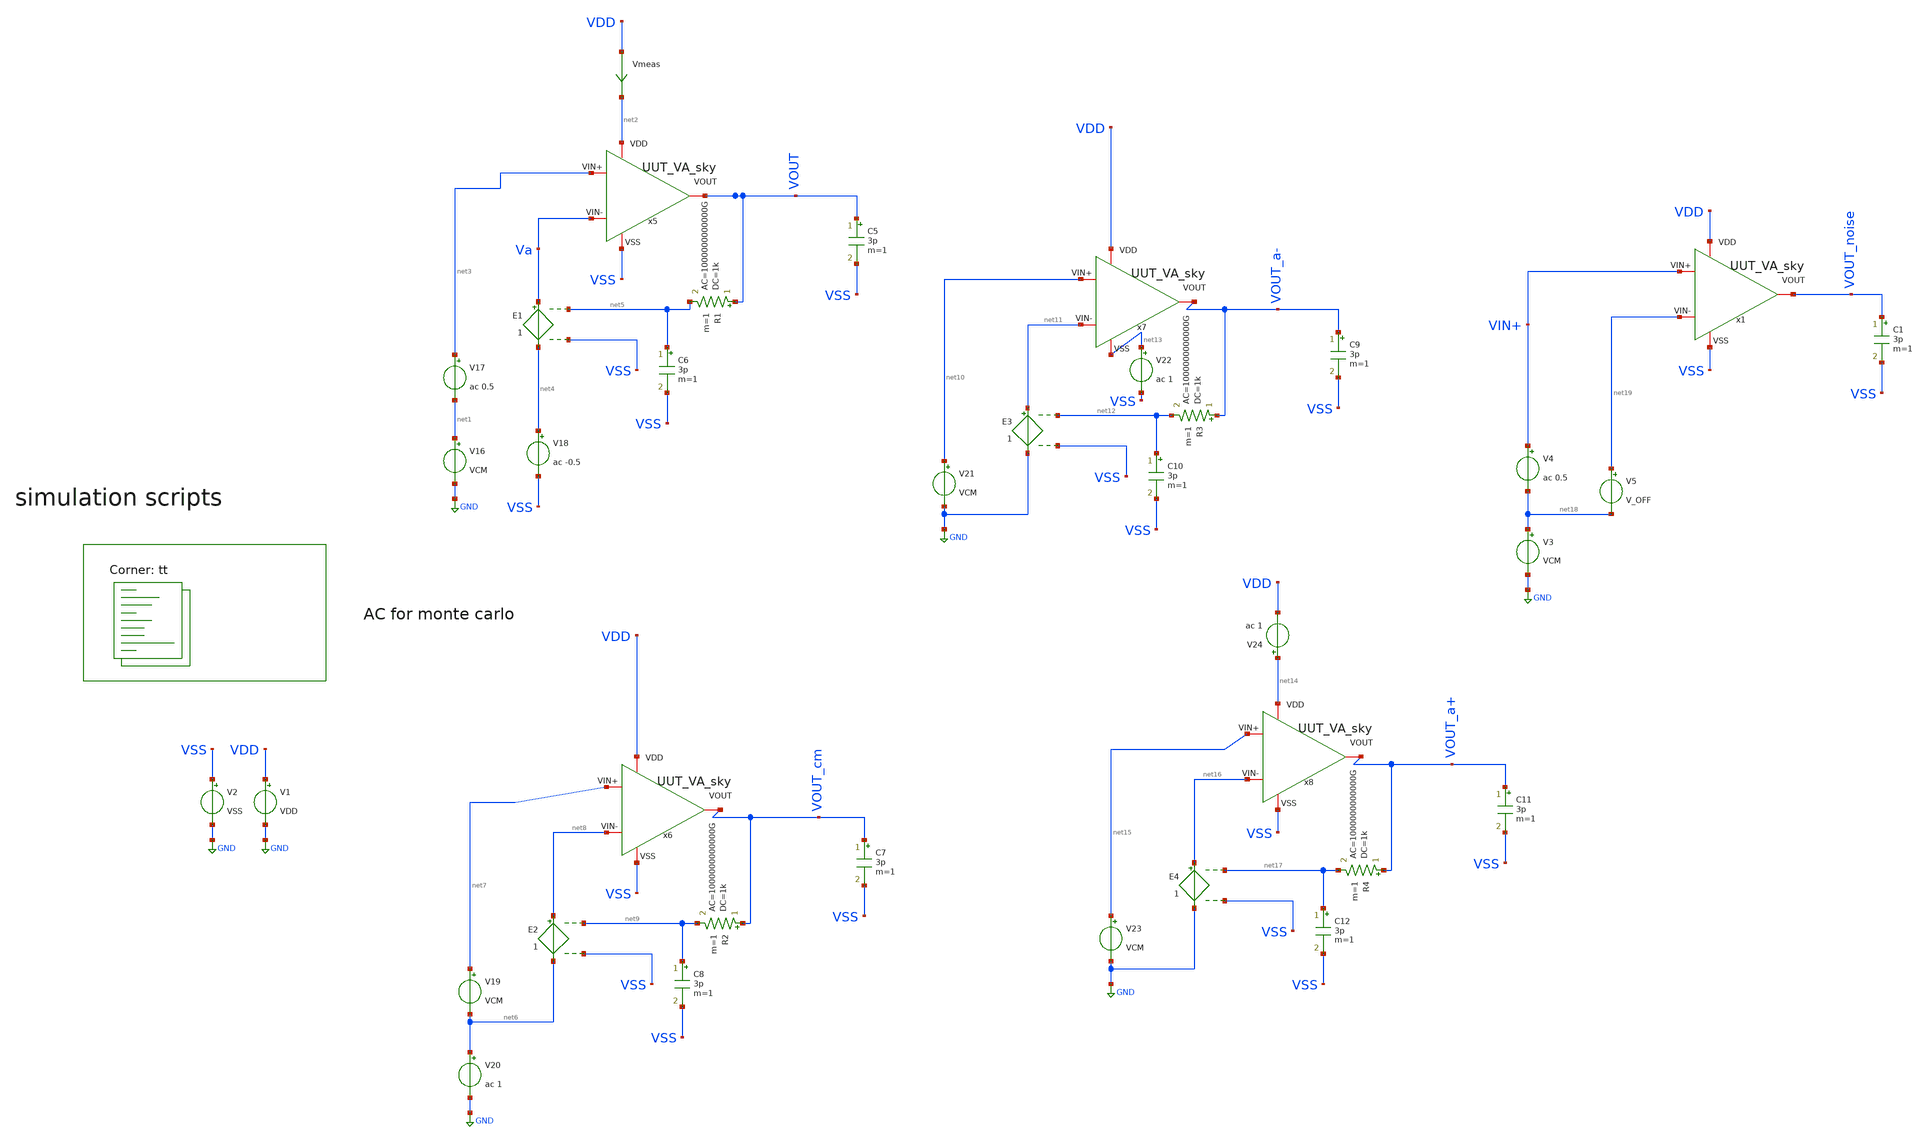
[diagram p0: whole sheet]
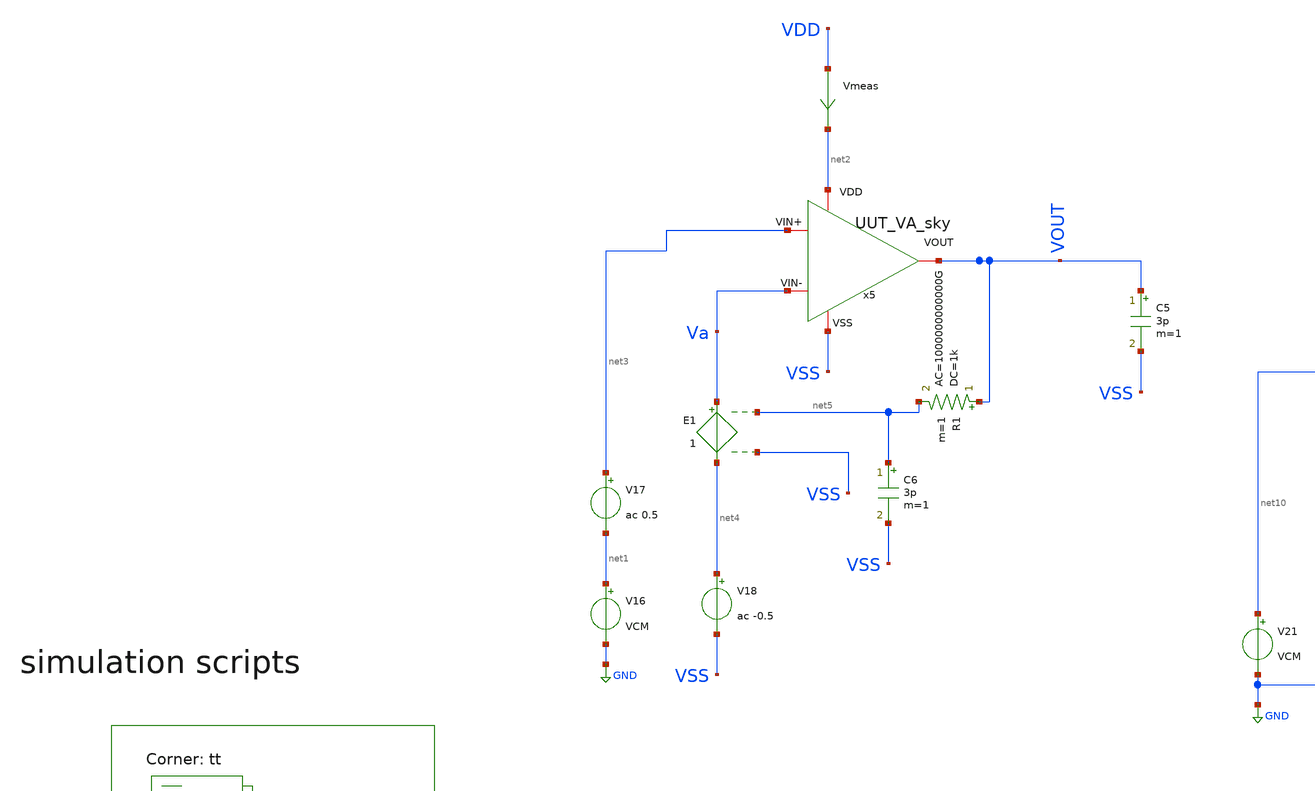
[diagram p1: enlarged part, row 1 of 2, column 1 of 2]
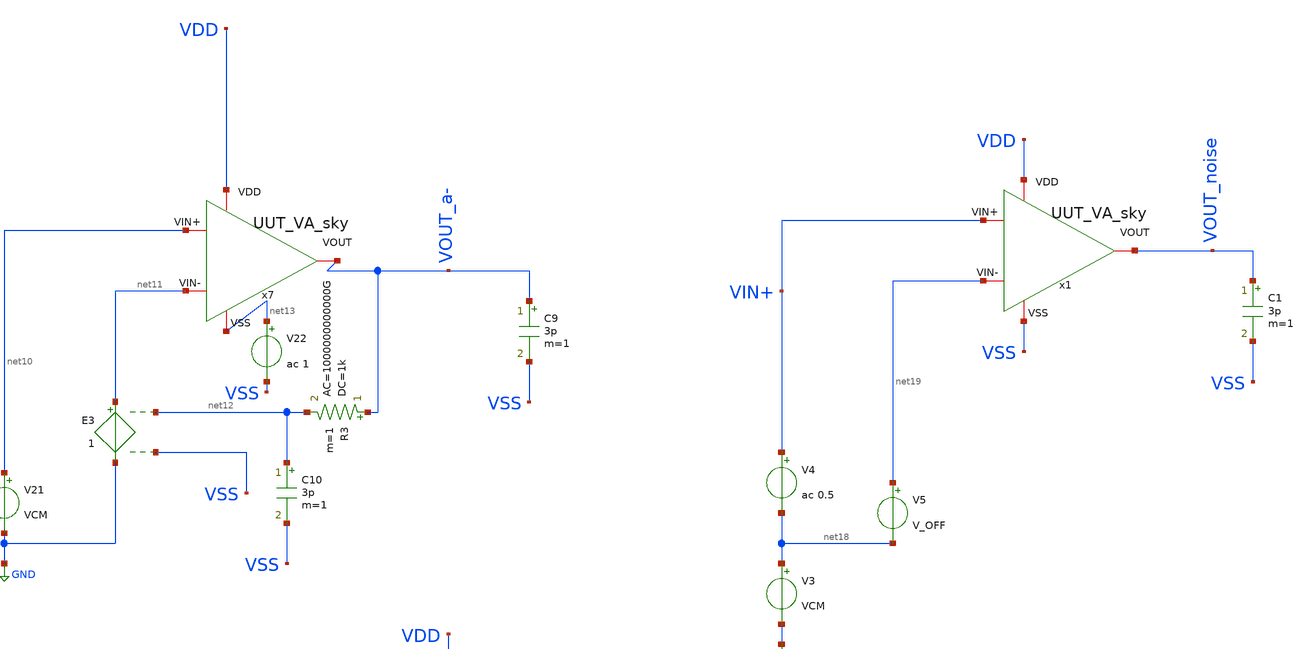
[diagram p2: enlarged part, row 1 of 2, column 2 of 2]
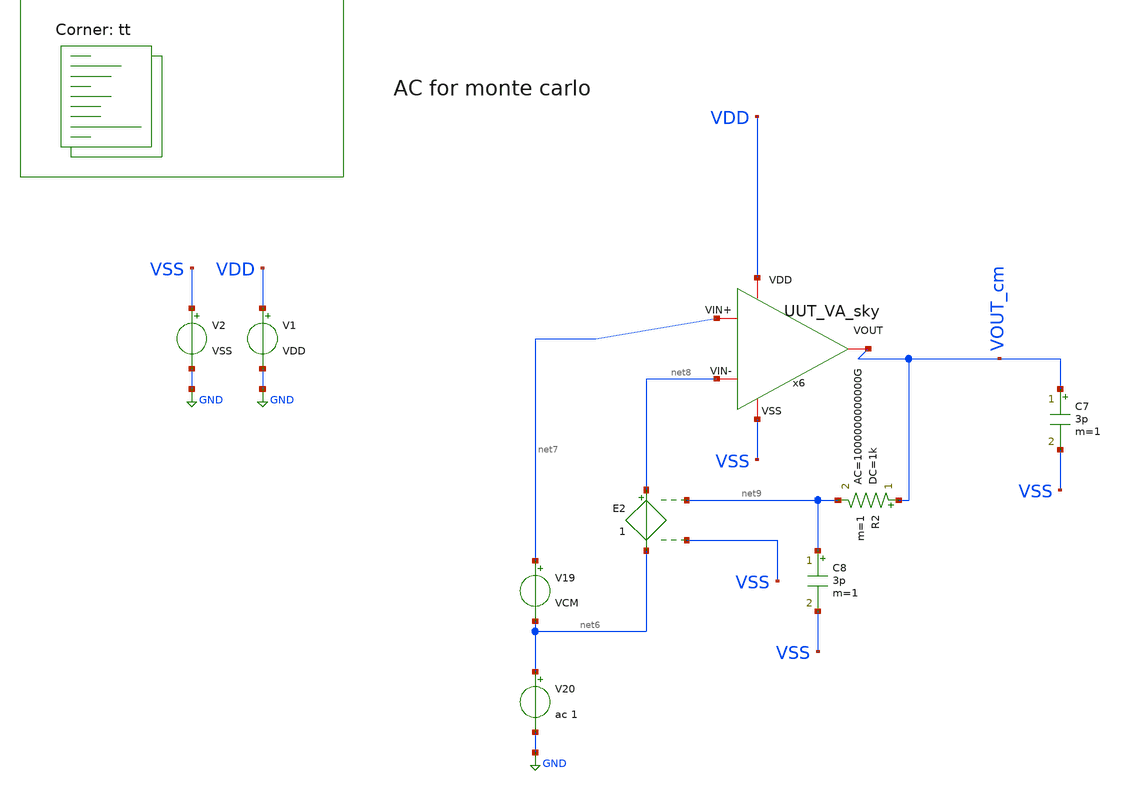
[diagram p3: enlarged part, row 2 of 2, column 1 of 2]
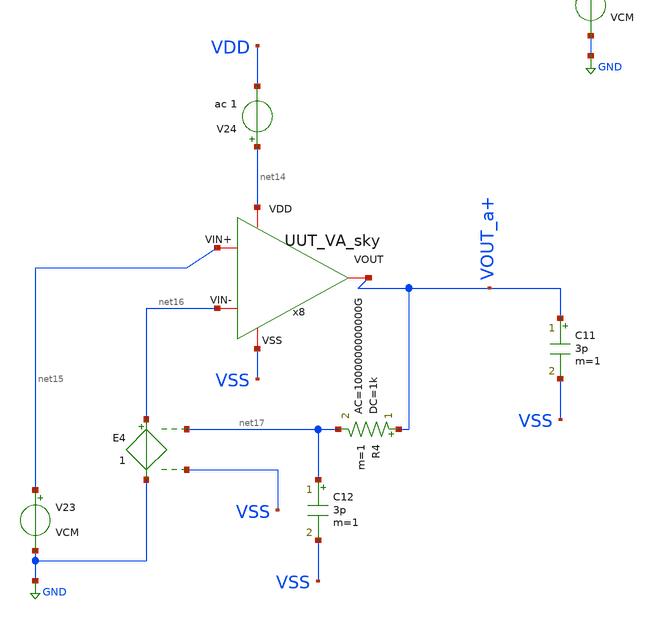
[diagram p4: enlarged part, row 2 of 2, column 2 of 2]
** sch_path: Learning/single_ended_amplifiers/Design_and_Analysis_of_Two-Stage_CMOS_Operational_Amplifier_for_Fluorescence_Signal_Processing_sky130_5V/amplifier_design/OTA_AC_TB.sch
**.subckt OTA_AC_TB
V1 VDD GND VDD
V2 VSS GND VSS
Vmeas VDD net2 0
.save i(vmeas)
x5 net2 VSS Va net3 VOUT UUT_VA_sky
C5 VOUT VSS 3p m=1
V16 net1 GND VCM
V17 net3 net1 ac 0.5
V18 net4 VSS ac -0.5
E1 Va net4 net5 VSS 1
R1 VOUT net5 1k ac=1000000000000G m=1
C6 net5 VSS 3p m=1
x6 VDD VSS net8 net7 VOUT_cm UUT_VA_sky
C7 VOUT_cm VSS 3p m=1
V19 net7 net6 VCM
V20 net6 GND ac 1
E2 net8 net6 net9 VSS 1
R2 VOUT_cm net9 1k ac=1000000000000G m=1
C8 net9 VSS 3p m=1
x7 VDD net13 net11 net10 VOUT_a- UUT_VA_sky
C9 VOUT_a- VSS 3p m=1
V21 net10 GND VCM
E3 net11 GND net12 VSS 1
R3 VOUT_a- net12 1k ac=1000000000000G m=1
C10 net12 VSS 3p m=1
V22 net13 VSS ac 1
x8 net14 VSS net16 net15 VOUT_a+ UUT_VA_sky
C11 VOUT_a+ VSS 3p m=1
V23 net15 GND VCM
E4 net16 GND net17 VSS 1
R4 VOUT_a+ net17 1k ac=1000000000000G m=1
C12 net17 VSS 3p m=1
V24 net14 VDD ac 1
x1 VDD VSS net19 VIN+ VOUT_noise UUT_VA_sky
V3 net18 GND VCM
V4 VIN+ net18 ac 0.5
V5 net19 net18 V_OFF
C1 VOUT_noise VSS 3p m=1
**** begin user architecture code
.lib $::SKYWATER_MODELS/sky130.lib.spice tt

.Temp 27
.param VDD = 5
.param VSS = 0
.param CL = 3p
.param V_OFF = -400u
.param VCM=2.5


.control

	save all
	ac dec 100 1 10G
	plot db(v(VOUT)) (180+(180*ph(v(VOUT))/pi))
	plot (db(v(VOUT)) - db(v(VOUT_CM)))
	plot (db(v(VOUT)) - db(v(VOUT_A-)))
	plot (db(v(VOUT))- db(v(VOUT_A+)))
	wrdata VIN_sweep_AC.csv db(v(VOUT)) phase(v(VOUT)) db(v(VOUT_CM)) db(v(VOUT_A-)) db(v(VOUT_A+))

	noise v(VOUT_noise,VSS) V4 dec 10 1 40000k
	print inoise_total
	print onoise_total
	setplot noise1

	plot onoise_spectrum
	plot inoise_spectrum
	op
	print (2.5-V(VOUT))
	print v(VOUT_noise)

.endc




**** end user architecture code
**.ends

* expanding   symbol:  Sky130A/UUT_sky/UUT_VA_sky.sym # of pins=5
** sym_path: my_ip/LIB/Sky130A/UUT_sky/UUT_VA_sky.sym
** sch_path: my_ip/LIB/Sky130A/UUT_sky/UUT_VA_sky.sch
.subckt UUT_VA_sky VDD VSS VIN- VIN+ VOUT
*.iopin VDD
*.iopin VSS
*.iopin VIN-
*.iopin VIN+
*.iopin VOUT
x1 VDD VSS VIN+ VIN- VOUT amplifier
.ends


* expanding   symbol:
*+  Sky130A/Learning/Design_of_Two-Stage_CMOS_Operational_Amplifier_for_Fluorescence_Signal_Processing_5V/amplifier.sym # of pins=5
** sym_path: my_ip/LIB/Sky130A/Learning/Design_of_Two-Stage_CMOS_Operational_Amplifier_for_Fluorescence_Signal_Processing_5V/amplifier.sym
** sch_path: my_ip/LIB/Sky130A/Learning/Design_of_Two-Stage_CMOS_Operational_Amplifier_for_Fluorescence_Signal_Processing_5V/amplifier.sch
.subckt amplifier VDD VSS Vin+ Vin- VOUT
*.iopin VDD
*.iopin VSS
*.iopin Vin+
*.iopin Vin-
*.iopin VOUT
XR2 VSS net2 VSS sky130_fd_pr__res_high_po_0p35 L=20.4 mult=1 m=1
XM7 net1 net1 VSS VSS sky130_fd_pr__nfet_g5v0d10v5 L=3.2 W='1 * 2 ' nf=2 ad='int((nf+1)/2) * W / nf * 0.29'
+ as='int((nf+2)/2) * W / nf * 0.29' pd='2*int((nf+1)/2) * (W / nf + 0.29)' ps='2*int((nf+2)/2) * (W / nf + 0.29)'
+ nrd='0.29 / W ' nrs='0.29 / W ' sa=0 sb=0 sd=0 mult=2 m=2
XM8 net3 net1 net2 VSS sky130_fd_pr__nfet_g5v0d10v5 L=3.2 W='1 * 8 ' nf=8 ad='int((nf+1)/2) * W / nf * 0.29'
+ as='int((nf+2)/2) * W / nf * 0.29' pd='2*int((nf+1)/2) * (W / nf + 0.29)' ps='2*int((nf+2)/2) * (W / nf + 0.29)'
+ nrd='0.29 / W ' nrs='0.29 / W ' sa=0 sb=0 sd=0 mult=2 m=2
XM9 VB1 VB2 net3 VSS sky130_fd_pr__nfet_g5v0d10v5 L=2 W='1 * 2 ' nf=2 ad='int((nf+1)/2) * W / nf * 0.29'
+ as='int((nf+2)/2) * W / nf * 0.29' pd='2*int((nf+1)/2) * (W / nf + 0.29)' ps='2*int((nf+2)/2) * (W / nf + 0.29)'
+ nrd='0.29 / W ' nrs='0.29 / W ' sa=0 sb=0 sd=0 mult=2 m=2
XM10 VB2 VB2 net1 VSS sky130_fd_pr__nfet_g5v0d10v5 L=2 W='1 * 2 ' nf=2 ad='int((nf+1)/2) * W / nf * 0.29'
+ as='int((nf+2)/2) * W / nf * 0.29' pd='2*int((nf+1)/2) * (W / nf + 0.29)' ps='2*int((nf+2)/2) * (W / nf + 0.29)'
+ nrd='0.29 / W ' nrs='0.29 / W ' sa=0 sb=0 sd=0 mult=2 m=2
XM2 net6 Vin- net4 net4 sky130_fd_pr__pfet_g5v0d10v5 L=1 W='4.5 * 2 ' nf=2 ad='int((2 + 1)/2) * 4.5 * 0.29'
+ as='int((2 + 2)/2) * 4.5 * 0.29' pd='2*int((2 + 1)/2) * (4.5 + 0.29)' ps='2*int((2 + 2)/2) * (4.5 + 0.29)'
+ nrd='0.29 / 4.5 / 2 ' nrs='0.29 / 4.5 / 2 ' sa=0 sb=0 sd=0 mult=4 m=4
XM3 net5 Vin+ net4 net4 sky130_fd_pr__pfet_g5v0d10v5 L=1 W='4.5 * 2 ' nf=2 ad='int((2 + 1)/2) * 4.5 * 0.29'
+ as='int((2 + 2)/2) * 4.5 * 0.29' pd='2*int((2 + 1)/2) * (4.5 + 0.29)' ps='2*int((2 + 2)/2) * (4.5 + 0.29)'
+ nrd='0.29 / 4.5 / 2 ' nrs='0.29 / 4.5 / 2 ' sa=0 sb=0 sd=0 mult=4 m=4
XM4 net5 net6 VSS VSS sky130_fd_pr__nfet_g5v0d10v5 L=2 W='1.5 * 2 ' nf=2 ad='int((nf+1)/2) * W / nf * 0.29'
+ as='int((nf+2)/2) * W / nf * 0.29' pd='2*int((nf+1)/2) * (W / nf + 0.29)' ps='2*int((nf+2)/2) * (W / nf + 0.29)'
+ nrd='0.29 / W ' nrs='0.29 / W ' sa=0 sb=0 sd=0 mult=2 m=2
XM11 net6 net6 VSS VSS sky130_fd_pr__nfet_g5v0d10v5 L=2 W='1.5 * 2 ' nf=2 ad='int((nf+1)/2) * W / nf * 0.29'
+ as='int((nf+2)/2) * W / nf * 0.29' pd='2*int((nf+1)/2) * (W / nf + 0.29)' ps='2*int((nf+2)/2) * (W / nf + 0.29)'
+ nrd='0.29 / W ' nrs='0.29 / W ' sa=0 sb=0 sd=0 mult=2 m=2
XM13 VOUT net5 VSS VSS sky130_fd_pr__nfet_g5v0d10v5 L=1 W='4 * 2 ' nf=2 ad='int((nf+1)/2) * W / nf * 0.29'
+ as='int((nf+2)/2) * W / nf * 0.29' pd='2*int((nf+1)/2) * (W / nf + 0.29)' ps='2*int((nf+2)/2) * (W / nf + 0.29)'
+ nrd='0.29 / W ' nrs='0.29 / W ' sa=0 sb=0 sd=0 mult=2 m=2
XM14 net7 VB2 net5 VSS sky130_fd_pr__nfet_g5v0d10v5 L=2 W='1.4 * 1 ' nf=1 ad='int((nf+1)/2) * W / nf * 0.29'
+ as='int((nf+2)/2) * W / nf * 0.29' pd='2*int((nf+1)/2) * (W / nf + 0.29)' ps='2*int((nf+2)/2) * (W / nf + 0.29)'
+ nrd='0.29 / W ' nrs='0.29 / W ' sa=0 sb=0 sd=0 mult=2 m=2
XC1 VOUT net7 sky130_fd_pr__cap_mim_m3_1 W=8 L=8 MF=4 m=4
XM1 VB2 VB1 VDD VDD sky130_fd_pr__pfet_g5v0d10v5 L=2.2 W='1 * 2 ' nf=2 ad='int((2 + 1)/2) * 1 * 0.29'
+ as='int((2 + 2)/2) * 1 * 0.29' pd='2*int((2 + 1)/2) * (1 + 0.29)' ps='2*int((2 + 2)/2) * (1 + 0.29)'
+ nrd='0.29 / 1 / 2 ' nrs='0.29 / 1 / 2 ' sa=0 sb=0 sd=0 mult=2 m=2
XM5 VB1 VB1 VDD VDD sky130_fd_pr__pfet_g5v0d10v5 L=2.2 W='1 * 2 ' nf=2 ad='int((2 + 1)/2) * 1 * 0.29'
+ as='int((2 + 2)/2) * 1 * 0.29' pd='2*int((2 + 1)/2) * (1 + 0.29)' ps='2*int((2 + 2)/2) * (1 + 0.29)'
+ nrd='0.29 / 1 / 2 ' nrs='0.29 / 1 / 2 ' sa=0 sb=0 sd=0 mult=2 m=2
XM6 net4 VB1 VDD VDD sky130_fd_pr__pfet_g5v0d10v5 L=2.2 W='1 * 2 ' nf=2 ad='int((2 + 1)/2) * 1 * 0.29'
+ as='int((2 + 2)/2) * 1 * 0.29' pd='2*int((2 + 1)/2) * (1 + 0.29)' ps='2*int((2 + 2)/2) * (1 + 0.29)'
+ nrd='0.29 / 1 / 2 ' nrs='0.29 / 1 / 2 ' sa=0 sb=0 sd=0 mult=8 m=8
XM12 VOUT VB1 VDD VDD sky130_fd_pr__pfet_g5v0d10v5 L=2.2 W='1 * 2 ' nf=2 ad='int((2 + 1)/2) * 1 * 0.29'
+ as='int((2 + 2)/2) * 1 * 0.29' pd='2*int((2 + 1)/2) * (1 + 0.29)' ps='2*int((2 + 2)/2) * (1 + 0.29)'
+ nrd='0.29 / 1 / 2 ' nrs='0.29 / 1 / 2 ' sa=0 sb=0 sd=0 mult=16 m=16
.ends

.GLOBAL GND
.end
